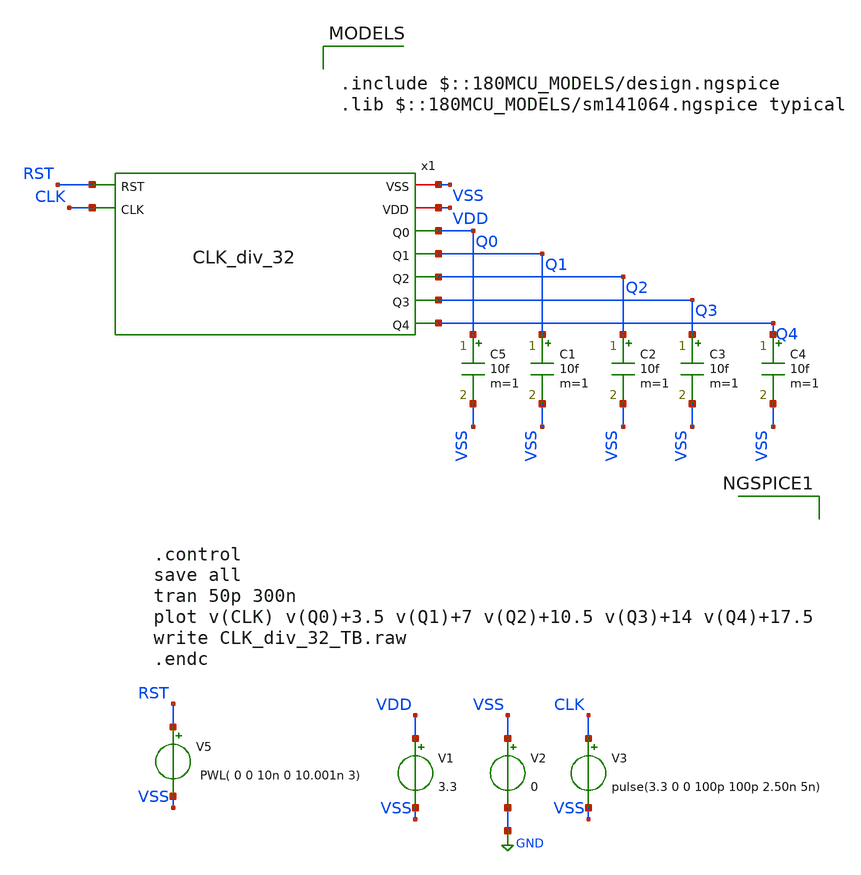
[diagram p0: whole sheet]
** sch_path: Clock_Generator_PAKISTAN_02/Schematics/CLK_div_32_TB.sch
**.subckt CLK_div_32_TB
V1 VDD VSS 3.3
V2 VSS GND 0
V3 CLK VSS pulse(3.3 0 0 100p 100p 2.50n 5n)
C5 Q0 VSS 10f m=1
C1 Q1 VSS 10f m=1
C2 Q2 VSS 10f m=1
C3 Q3 VSS 10f m=1
C4 Q4 VSS 10f m=1
x1 VSS VDD Q0 Q1 Q2 Q3 Q4 RST CLK CLK_div_32
V5 RST VSS PWL( 0 0 10n 0 10.001n 3)
**** begin user architecture code

.include $::180MCU_MODELS/design.ngspice
.lib $::180MCU_MODELS/sm141064.ngspice typical




.control
save all
tran 50p 300n
plot v(CLK) v(Q0)+3.5 v(Q1)+7 v(Q2)+10.5 v(Q3)+14 v(Q4)+17.5
write CLK_div_32_TB.raw
.endc


**** end user architecture code
**.ends
.GLOBAL GND
.end
